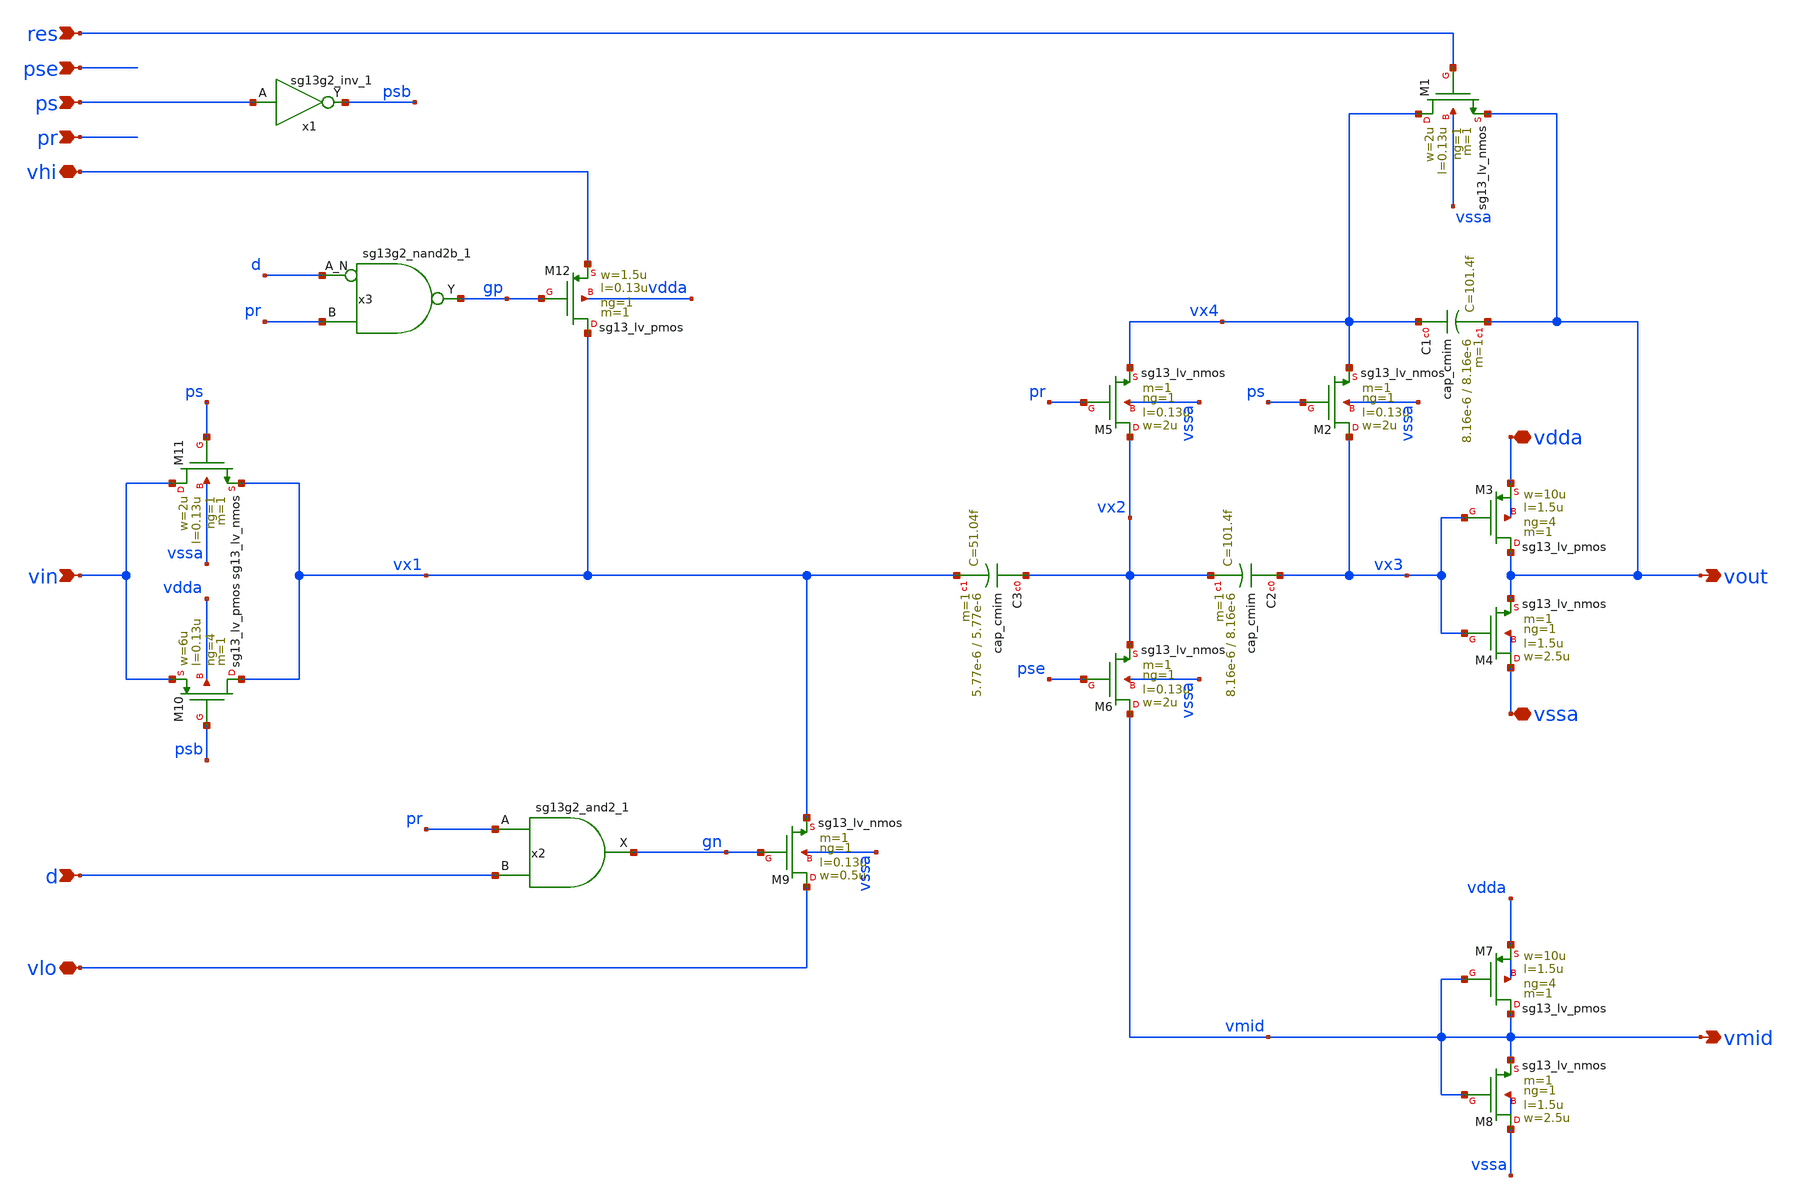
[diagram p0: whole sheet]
** sch_path: 5_Design/4_Layout/Team 5/splitUpSimulationsAndSchematics/integ_5.sch
* IHP-GmbH/IHP-Open-PDK/ihp-sg13g2/libs.tech/xschem/sg13g2_stdcells/sg13g2_nand2b_1.sch:
* Copyright 2023 IHP PDK Authors
* Licensed under the Apache License, Version 2.0 (the "License");
**.subckt integ_5 res pse ps pr vssa vdda vout vmid d vlo vin vhi
*.ipin res
*.ipin pse
*.ipin ps
*.ipin pr
*.iopin vssa
*.iopin vdda
*.opin vout
*.opin vmid
*.ipin d
*.iopin vlo
*.ipin vin
*.iopin vhi
x1 psb ps VDD VSS sg13g2_inv_1
XM1 vx4 res vout vssa sg13_lv_nmos w=2u l=0.13u ng=1 m=1 mm_ok=1
XC1 vx4 vout cap_cmim w=8.16e-6 l=8.16e-6 m=1 mm_ok=1
XM2 vx3 ps vx4 vssa sg13_lv_nmos w=2u l=0.13u ng=1 m=1 mm_ok=1
XM3 vout vx3 vdda vdda sg13_lv_pmos w=10u l=1.5u ng=4 m=1 mm_ok=1
XM4 vssa vx3 vout vssa sg13_lv_nmos w=2.5u l=1.5u ng=1 m=1 mm_ok=1
XC2 vx3 vx2 cap_cmim w=8.16e-6 l=8.16e-6 m=1 mm_ok=1
XM5 vx2 pr vx4 vssa sg13_lv_nmos w=2u l=0.13u ng=1 m=1 mm_ok=1
XM6 vmid pse vx2 vssa sg13_lv_nmos w=2u l=0.13u ng=1 m=1 mm_ok=1
XM7 vmid vmid vdda vdda sg13_lv_pmos w=10u l=1.5u ng=4 m=1 mm_ok=1
XM8 vssa vmid vmid vssa sg13_lv_nmos w=2.5u l=1.5u ng=1 m=1 mm_ok=1
XM9 vlo gn vx1 vssa sg13_lv_nmos w=0.5u l=0.13u ng=1 m=1 mm_ok=1
XC3 vx2 vx1 cap_cmim w=5.77e-6 l=5.77e-6 m=1 mm_ok=1
x2 gn pr d VDD VSS sg13g2_and2_1
XM10 vx1 psb vin vdda sg13_lv_pmos w=6u l=0.13u ng=4 m=1 mm_ok=1
XM11 vin ps vx1 vssa sg13_lv_nmos w=2u l=0.13u ng=1 m=1 mm_ok=1
x3 gp d pr VDD VSS sg13g2_nand2b_1
XM12 vx1 gp vhi vdda sg13_lv_pmos w=1.5u l=0.13u ng=1 m=1 mm_ok=1
**.ends

* expanding   symbol:  sg13g2_stdcells/sg13g2_inv_1.sym # of pins=2
** sym_path: sg13g2_stdcells/sg13g2_inv_1.sym
** sch_path: sg13g2_stdcells/sg13g2_inv_1.sch
.subckt sg13g2_inv_1 Y A VDD VSS
*.opin Y
*.ipin A
*.iopin VDD
*.iopin VSS
XM1 Y A VSS VSS sg13_lv_nmos w=740.00n l=130.00n ng=1 m=1 mm_ok=1
XM2 Y A VDD VDD sg13_lv_pmos w=1.12u l=130.00n ng=1 m=1 mm_ok=1
.ends


* expanding   symbol:  sg13g2_stdcells/sg13g2_and2_1.sym # of pins=3
** sym_path: sg13g2_stdcells/sg13g2_and2_1.sym
** sch_path: sg13g2_stdcells/sg13g2_and2_1.sch
.subckt sg13g2_and2_1 X A B VDD VSS
*.ipin A
*.ipin B
*.opin X
*.iopin VDD
*.iopin VSS
XM1 net1 A net2 VSS sg13_lv_nmos w=640.00n l=130.00n ng=1 m=1 mm_ok=1
XM2 net2 B VSS VSS sg13_lv_nmos w=640.00n l=130.00n ng=1 m=1 mm_ok=1
XM3 X net1 VSS VSS sg13_lv_nmos w=740.00n l=130.00n ng=1 m=1 mm_ok=1
XM4 net1 B VDD VDD sg13_lv_pmos w=840.00n l=130.00n ng=1 m=1 mm_ok=1
XM5 net1 A VDD VDD sg13_lv_pmos w=840.00n l=130.00n ng=1 m=1 mm_ok=1
XM6 X net1 VDD VDD sg13_lv_pmos w=1.12u l=130.00n ng=1 m=1 mm_ok=1
.ends


* expanding   symbol:  sg13g2_stdcells/sg13g2_nand2b_1.sym # of pins=3
** sym_path: sg13g2_stdcells/sg13g2_nand2b_1.sym
** sch_path: sg13g2_stdcells/sg13g2_nand2b_1.sch
.subckt sg13g2_nand2b_1 Y A_N B VDD VSS
*.opin Y
*.ipin B
*.ipin A_N
*.iopin VDD
*.iopin VSS
XM1 net1 A_N VSS VSS sg13_lv_nmos w=550.00n l=130.00n ng=1 m=1 mm_ok=1
XM2 Y net1 net2 VSS sg13_lv_nmos w=740.00n l=130.00n ng=1 m=1 mm_ok=1
XM3 net2 B VSS VSS sg13_lv_nmos w=740.00n l=130.00n ng=1 m=1 mm_ok=1
XM4 Y B VDD VDD sg13_lv_pmos w=1.12u l=130.00n ng=1 m=1 mm_ok=1
XM5 net1 A_N VDD VDD sg13_lv_pmos w=840.00n l=130.00n ng=1 m=1 mm_ok=1
XM6 Y net1 VDD VDD sg13_lv_pmos w=1.12u l=130.00n ng=1 m=1 mm_ok=1
.ends

.end
